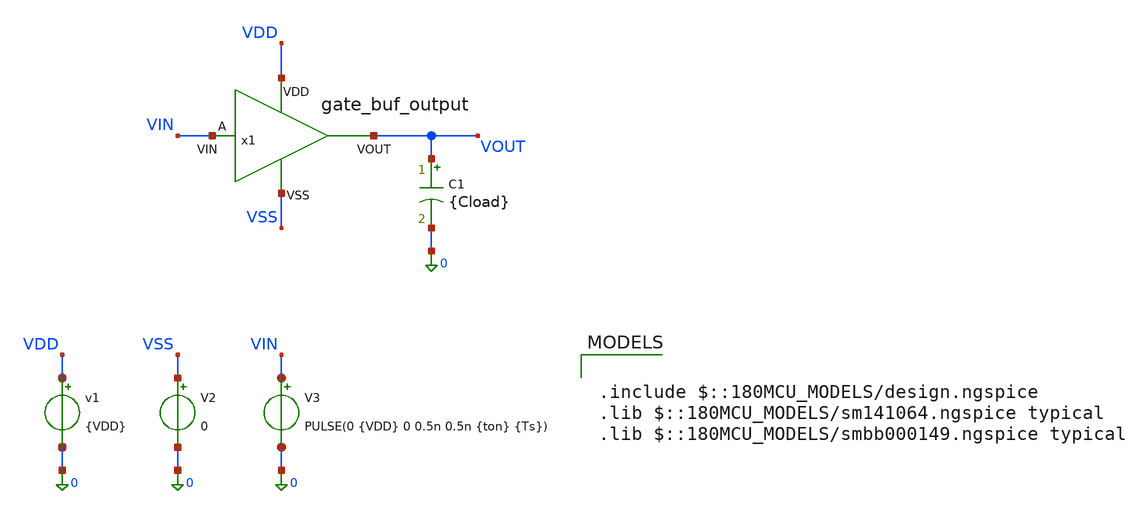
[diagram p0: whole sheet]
** sch_path: designs/sar_adc/digital/gate_buf_output/xschem/tb_buf_output.sch
**.subckt tb_buf_output
V2 VSS 0 0
C1 VOUT 0 {Cload} m=1
v1 VDD 0 {VDD}
V3 VIN 0 PULSE(0 {VDD} 0 0.5n 0.5n {ton} {Ts})
x1 VDD VIN VOUT VSS gate_buf_output
**** begin user architecture code

.include $::180MCU_MODELS/design.ngspice
.lib $::180MCU_MODELS/sm141064.ngspice typical
.lib $::180MCU_MODELS/smbb000149.ngspice typical



.param Vmid = 1.65
* Sampling clock
.param Fs = 16Meg

* Input parameters
.param Ts = 1/Fs
.param ton = Ts/2

.param Ns = 1024
.param Nc = 103
.param fin = Nc/Ns*Fs

.param sw_stat_mismatch = 0
.param fnoicor = 0

* Test-bench parameters
.temp 27
.param VDD = 3.3
.param Cload = 20p

.save @v.x1.V_inv1[i]
.save @v.x1.V_inv2[i]
.save @v.x1.V_inv3[i]
.save @v.x1.V_inv4[i]
.save all

.control

let tstep = 100p
let tstop = 0.2u

tran $&tstep $&tstop

* - Propagation delay
meas TRAN TPLH  TRIG v(vin) VAL=1.65 RISE=2 TARG v(vout) VAL=1.65 RISE=2
meas TRAN TPHL TRIG v(vin) VAL=1.65 FALL=2  TARG v(vout) VAL=1.65 FALL=2

* - Rise and fall time
meas TRAN TRISE  TRIG v(vout) VAL=0.33 RISE=2 TARG v(vout) VAL=2.97 RISE=2
meas TRAN TFALL  TRIG v(vout) VAL=2.97 FALL=2 TARG v(vout) VAL=0.33 FALL=2

* - Output voltage levels
meas TRAN VOH MAX v(vout) FROM=100n TO=0.2u
meas TRAN VOL MIN v(vout) FROM=100n TO=0.2u

* - Pulse width
meas TRAN PW_IN TRIG v(vin) VAL=1.65 RISE=2 TARG v(vin) VAL=1.65 FALL=2
meas TRAN PW_OUT TRIG v(vout) VAL=1.65 RISE=2 TARG v(vout) VAL=1.65 FALL=2

* - Average propagation delay
let TP_AVG = (TPLH + TPHL)/2

* - Power and Current calculations
let IDD = -1 * i(v1)
meas tran I_AVG AVG IDD FROM=100n TO=0.2u
let P_AVG = I_AVG * 3.3


*Internal currents
let I_inv1 = @v.x1.V_inv1[i]
let I_inv2 = @v.x1.V_inv2[i]
let I_inv3 = @v.x1.V_inv3[i]
let I_inv4 = @v.x1.V_inv4[i]

meas tran I_avg_inv1 AVG I_inv1 from=10p to=tstop
meas tran I_avg_inv2 AVG I_inv2 from=10p to=tstop
meas tran I_avg_inv3 AVG I_inv3 from=10p to=tstop
meas tran I_avg_inv4 AVG I_inv4 from=10p to=tstop
print I_avg_inv1 I_avg_inv2 I_avg_inv3 I_avg_inv4



* - Print results
print TPLH TPHL TP_AVG
print TRISE TFALL
print VOH VOL
print PW_IN PW_OUT
print I_AVG P_AVG

plot v(vout) v(vin)

.endc



**** end user architecture code
**.ends

* expanding   symbol:  designs/sar_adc/digital/gate_buf_output/xschem/gate_buf_output.sym # of
*+ pins=4
** sym_path: designs/sar_adc/digital/gate_buf_output/xschem/gate_buf_output.sym
** sch_path: designs/sar_adc/digital/gate_buf_output/xschem/gate_buf_output.sch
.subckt gate_buf_output VDD VIN VOUT VSS
*.iopin VDD
*.iopin VSS
*.iopin VIN
*.iopin VOUT
XMN1 net2 VIN VSS VSS nfet_03v3 L=0.28u W=2u nf=1 ad='int((nf+1)/2) * W/nf * 0.18u' as='int((nf+2)/2) * W/nf * 0.18u'
+ pd='2*int((nf+1)/2) * (W/nf + 0.18u)' ps='2*int((nf+2)/2) * (W/nf + 0.18u)' nrd='0.18u / W' nrs='0.18u / W'
+ sa=0 sb=0 sd=0 m=1
XMP1 net2 VIN net1 net1 pfet_03v3 L=0.28u W=6u nf=1 ad='int((nf+1)/2) * W/nf * 0.18u' as='int((nf+2)/2) * W/nf * 0.18u'
+ pd='2*int((nf+1)/2) * (W/nf + 0.18u)' ps='2*int((nf+2)/2) * (W/nf + 0.18u)' nrd='0.18u / W' nrs='0.18u / W'
+ sa=0 sb=0 sd=0 m=1
XMP2 net3 net2 net4 net4 pfet_03v3 L=0.28u W=6u nf=1 ad='int((nf+1)/2) * W/nf * 0.18u' as='int((nf+2)/2) * W/nf * 0.18u'
+ pd='2*int((nf+1)/2) * (W/nf + 0.18u)' ps='2*int((nf+2)/2) * (W/nf + 0.18u)' nrd='0.18u / W' nrs='0.18u / W'
+ sa=0 sb=0 sd=0 m=4
XMN2 net3 net2 VSS VSS nfet_03v3 L=0.28u W=2u nf=1 ad='int((nf+1)/2) * W/nf * 0.18u' as='int((nf+2)/2) * W/nf * 0.18u'
+ pd='2*int((nf+1)/2) * (W/nf + 0.18u)' ps='2*int((nf+2)/2) * (W/nf + 0.18u)' nrd='0.18u / W' nrs='0.18u / W'
+ sa=0 sb=0 sd=0 m=4
XMP3 net5 net3 net6 net6 pfet_03v3 L=0.28u W=6u nf=1 ad='int((nf+1)/2) * W/nf * 0.18u' as='int((nf+2)/2) * W/nf * 0.18u'
+ pd='2*int((nf+1)/2) * (W/nf + 0.18u)' ps='2*int((nf+2)/2) * (W/nf + 0.18u)' nrd='0.18u / W' nrs='0.18u / W'
+ sa=0 sb=0 sd=0 m=16
XMN3 net5 net3 VSS VSS nfet_03v3 L=0.28u W=2u nf=1 ad='int((nf+1)/2) * W/nf * 0.18u' as='int((nf+2)/2) * W/nf * 0.18u'
+ pd='2*int((nf+1)/2) * (W/nf + 0.18u)' ps='2*int((nf+2)/2) * (W/nf + 0.18u)' nrd='0.18u / W' nrs='0.18u / W'
+ sa=0 sb=0 sd=0 m=16
XMP4 VOUT net5 net7 net7 pfet_03v3 L=0.28u W=6u nf=1 ad='int((nf+1)/2) * W/nf * 0.18u' as='int((nf+2)/2) * W/nf * 0.18u'
+ pd='2*int((nf+1)/2) * (W/nf + 0.18u)' ps='2*int((nf+2)/2) * (W/nf + 0.18u)' nrd='0.18u / W' nrs='0.18u / W'
+ sa=0 sb=0 sd=0 m=64
XMN4 VOUT net5 VSS VSS nfet_03v3 L=0.28u W=2u nf=1 ad='int((nf+1)/2) * W/nf * 0.18u' as='int((nf+2)/2) * W/nf * 0.18u'
+ pd='2*int((nf+1)/2) * (W/nf + 0.18u)' ps='2*int((nf+2)/2) * (W/nf + 0.18u)' nrd='0.18u / W' nrs='0.18u / W'
+ sa=0 sb=0 sd=0 m=64
V_inv1 VDD net1 0
V_inv2 VDD net4 0
V_inv3 VDD net6 0
V_inv4 VDD net7 0
.ends

.end
